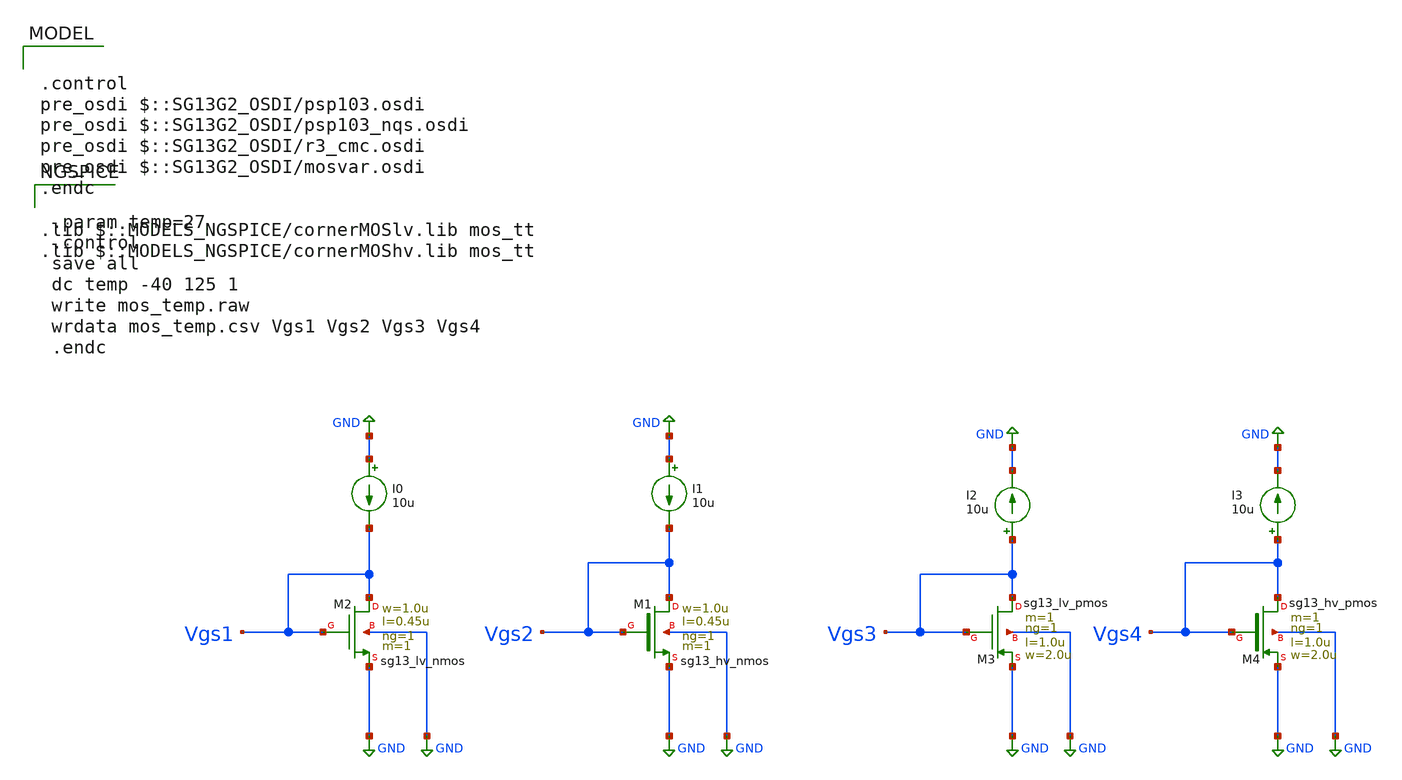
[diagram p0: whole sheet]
** sch_path: ihp-sg13g2/xschem_libs/sg13g2_tests/dc_mos_cs_temp/schematic/dc_mos_cs_temp.sch
* Copyright 2023 IHP PDK Authors
**.subckt dc_mos_cs_temp
XM3 Vgs3 Vgs3 GND GND sg13_lv_pmos w=2.0u l=1.0u ng=1 m=1 mm_ok=1
XM4 Vgs4 Vgs4 GND GND sg13_hv_pmos w=2.0u l=1.0u ng=1 m=1 mm_ok=1
I0 GND Vgs1 10u
I1 GND Vgs2 10u
I2 Vgs3 GND 10u
I3 Vgs4 GND 10u
XM1 Vgs2 Vgs2 GND GND sg13_hv_nmos w=1.0u l=0.45u ng=1 m=1 mm_ok=1
XM2 Vgs1 Vgs1 GND GND sg13_lv_nmos w=1.0u l=0.45u ng=1 m=1 mm_ok=1
**** begin user architecture code

.control
pre_osdi $::SG13G2_OSDI/psp103.osdi
pre_osdi $::SG13G2_OSDI/psp103_nqs.osdi
pre_osdi $::SG13G2_OSDI/r3_cmc.osdi
pre_osdi $::SG13G2_OSDI/mosvar.osdi
.endc

.lib $::MODELS_NGSPICE/cornerMOSlv.lib mos_tt
.lib $::MODELS_NGSPICE/cornerMOShv.lib mos_tt



.param temp=27
.control
save all
dc temp -40 125 1
write mos_temp.raw
wrdata mos_temp.csv Vgs1 Vgs2 Vgs3 Vgs4
.endc


**** end user architecture code
**.ends
.GLOBAL GND
.end
